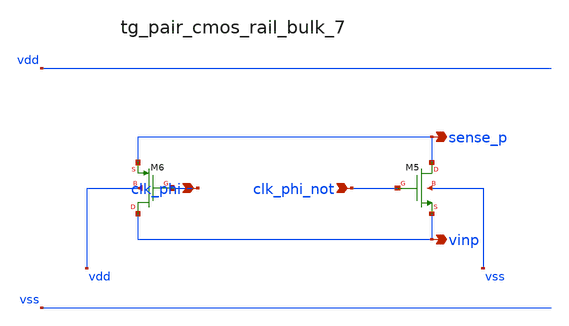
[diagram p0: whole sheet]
** sch_path: analog-db/raw/cmfb_004_output_switched_cap/hier/blocks/tg_pair_cmos_rail_bulk_7.sch
**.subckt tg_pair_cmos_rail_bulk_7 clk_phi clk_phi_not sense_p vinp
*.ipin clk_phi
*.ipin clk_phi_not
*.opin sense_p
*.opin vinp
XM5 sense_p clk_phi_not vinp vss sg13_lv_nmos w=x_dut_xm5_w l=x_dut_xm5_l ng=1 m=x_dut_xm5_m
XM6 vinp clk_phi sense_p vdd sg13_lv_pmos w=x_dut_xm6_w l=x_dut_xm6_l ng=1 m=x_dut_xm6_m
**.ends
.end
